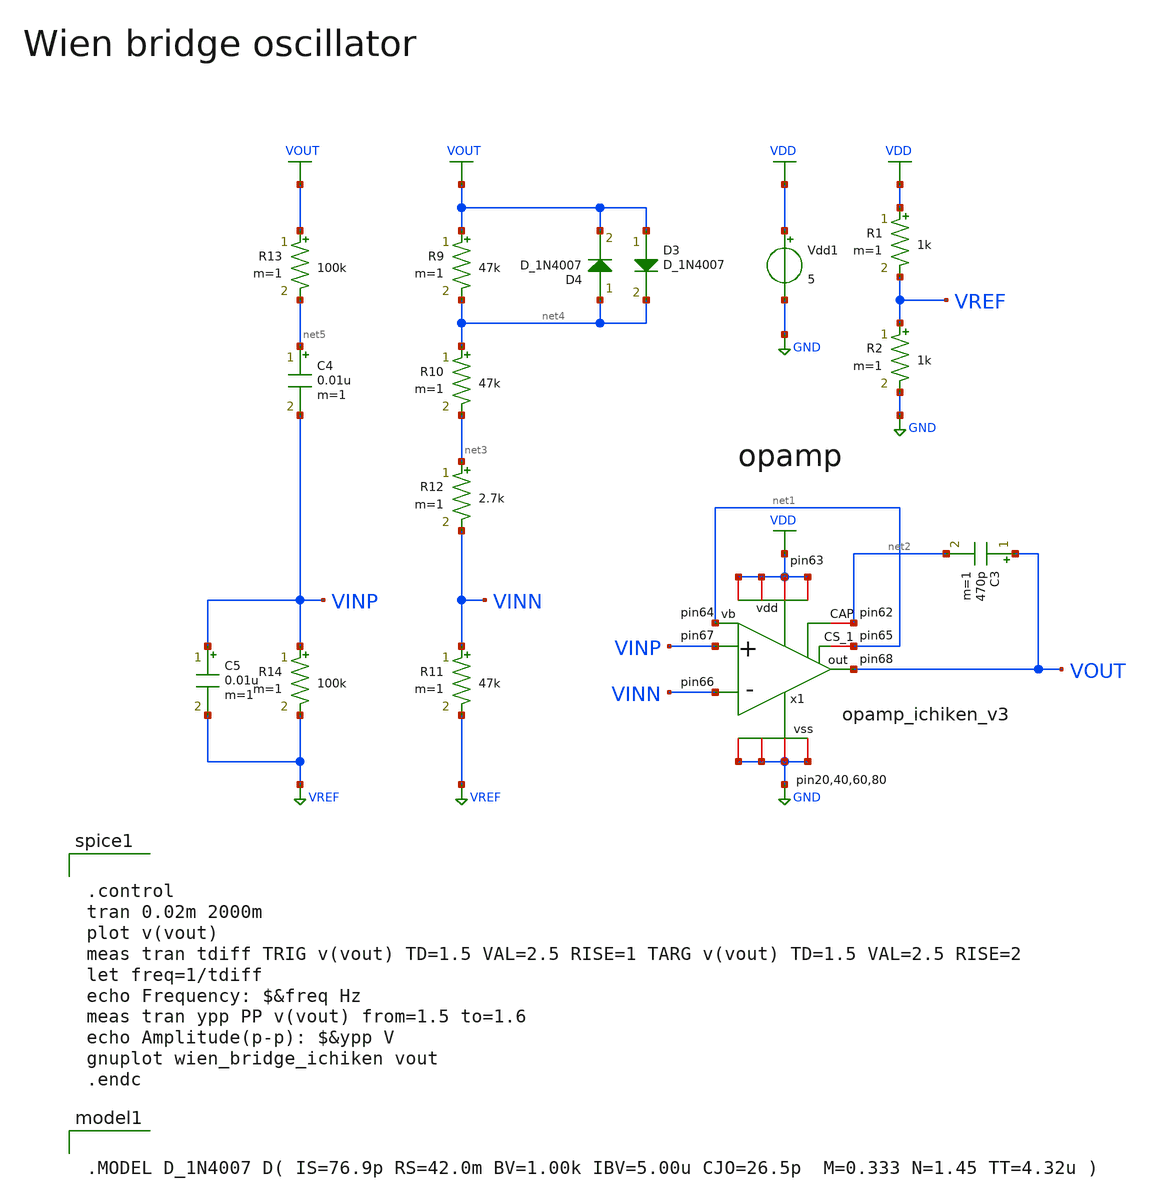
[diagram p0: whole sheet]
** sch_path: Vol.2/files/08/xschem/tb_wien_bridge_ichiken.sch
**.subckt tb_wien_bridge_ichiken
x1 VDD net1 GND VINP VINN net1 VOUT net2 opamp_ichiken_v3
C3 VOUT net2 470p m=1
Vdd1 VDD GND 5
R9 VOUT net4 47k m=1
R10 net4 net3 47k m=1
R11 VINN VREF 47k m=1
R12 net3 VINN 2.7k m=1
R13 VOUT net5 100k m=1
C4 net5 VINP 0.01u m=1
R14 VINP VREF 100k m=1
C5 VINP VREF 0.01u m=1
D3 VOUT net4 D_1N4007 area=1
D4 net4 VOUT D_1N4007 area=1
R1 VDD VREF 1k m=1
R2 VREF GND 1k m=1
**** begin user architecture code
 .include $::LIB/mos.lib
.include $::LIB/passive.lib
.include $::LIB/diode.lib


.control
tran 0.02m 2000m
plot v(vout)
meas tran tdiff TRIG v(vout) TD=1.5 VAL=2.5 RISE=1 TARG v(vout) TD=1.5 VAL=2.5 RISE=2
let freq=1/tdiff
echo Frequency: $&freq Hz
meas tran ypp PP v(vout) from=1.5 to=1.6
echo Amplitude(p-p): $&ypp V
gnuplot wien_bridge_ichiken vout
.endc




.MODEL D_1N4007 D( IS=76.9p RS=42.0m BV=1.00k IBV=5.00u CJO=26.5p  M=0.333 N=1.45 TT=4.32u )


**** end user architecture code
**.ends

* expanding   symbol:  ichiken/opamp_ichiken_v3.sym # of pins=14
** sym_path: Vol.2/files/08/xschem/ichiken/opamp_ichiken_v3.sym
** sch_path: Vol.2/files/08/xschem/ichiken/opamp_ichiken_v3.sch
.subckt opamp_ichiken_v3 vdd CS_1 vss vinp vinn vb out CAP
*.iopin vdd
*.iopin vss
*.ipin vinn
*.ipin vinp
*.ipin vb
*.opin cap
*.iopin vdd
*.iopin vss
*.iopin vss
*.iopin vdd
*.iopin vss
*.iopin vdd
*.iopin vss
*.opin out
*.iopin CS_1
M4 net2 net2 vdd vdd pmos L=4u W=100u m=1
M3 net1 net2 vdd vdd pmos L=4u W=100u m=1
M2 net2 net1 net3 vss nmos L=4u W=20u m=1
M1 net1 net3 vss vss nmos L=4u W=20u m=1
M5 net4 net2 vdd vdd pmos L=4u W=100u m=1
M6 net4 net4 vss vss nmos L=4u W=20u m=1
M7 CS_1 net4 vss vss nmos L=4u W=20u m=1
M8 net1 vdd vdd vdd pmos L=4u W=24u m=1
M9 net1 vdd vdd vdd pmos L=4u W=24u m=1
M10 net1 vdd vdd vdd pmos L=4u W=24u m=1
M11 net1 vdd vdd vdd pmos L=4u W=24u m=1
M13 net2 vdd vdd vdd pmos L=4u W=24u m=1
M12 net2 vdd vdd vdd pmos L=4u W=24u m=1
M15 net2 vdd vdd vdd pmos L=4u W=24u m=1
M16 net2 vdd vdd vdd pmos L=4u W=24u m=1
M24 net4 vdd vdd vdd pmos L=4u W=24u m=1
M25 net4 vdd vdd vdd pmos L=4u W=24u m=1
M26 net4 vss vss vss nmos L=4u W=10u m=1
M27 net4 vss vss vss nmos L=4u W=10u m=1
M29 CS_1 vss vss vss nmos L=4u W=10u m=1
M30 CS_1 vss vss vss nmos L=4u W=10u m=1
M28 net7 vb vdd vdd pmos L=4u W=80u m=1
M31 net6 vinn net7 net7 pmos L=4u W=400u m=1
M32 net5 vinp net7 net7 pmos L=4u W=400u m=1
M33 net6 net6 vss vss nmos L=4u W=60u m=1
M35 net7 vdd vdd vdd pmos L=4u W=20u m=1
M36 net7 vdd vdd vdd pmos L=4u W=20u m=1
M37 net5 net7 net7 net7 pmos L=4u W=20u m=1
M38 net5 net7 net7 net7 pmos L=4u W=20u m=1
M39 net6 net7 net7 net7 pmos L=4u W=20u m=1
M40 net6 net7 net7 net7 pmos L=4u W=20u m=1
M41 net5 net7 net7 net7 pmos L=4u W=20u m=1
M42 net5 net7 net7 net7 pmos L=4u W=20u m=1
M43 net6 net7 net7 net7 pmos L=4u W=20u m=1
M44 net6 net7 net7 net7 pmos L=4u W=20u m=1
M45 net6 vss vss vss nmos L=4u W=20u m=1
M46 net6 vss vss vss nmos L=4u W=20u m=1
M47 net5 vss vss vss nmos L=4u W=20u m=1
M48 net5 vss vss vss nmos L=4u W=20u m=1
M49 vb vb vdd vdd pmos L=4u W=80u m=1
M51 net8 net8 net9 vss nmos L=4u W=25u m=1
M52 net9 net9 vss vss nmos L=4u W=25u m=1
M53 out vb vdd vdd pmos L=4u W=140u m=1
M54 out net5 vss vss nmos L=4u W=200u m=1
M55 net5 net6 vss vss nmos L=4u W=60u m=1
M56 cap net8 net5 vss nmos L=4u W=40u m=1
R1 vss net3 HR_poly W=5 L=70
M20 net2 net3 net3 vss nmos L=4u W=10u m=1
M21 net2 net3 net3 vss nmos L=4u W=10u m=1
M22 net2 net3 net3 vss nmos L=4u W=10u m=1
M23 net2 net3 net3 vss nmos L=4u W=10u m=1
M14 net1 vss vss vss nmos L=4u W=10u m=1
M17 net1 vss vss vss nmos L=4u W=10u m=1
M18 net1 vss vss vss nmos L=4u W=10u m=1
M19 net1 vss vss vss nmos L=4u W=10u m=1
M50 net8 vb vdd vdd pmos L=4u W=80u m=1
C2 out cap poly_cap W=65 L=65
.ends

.GLOBAL GND
.GLOBAL VDD
.GLOBAL VREF
.GLOBAL VOUT
.end
